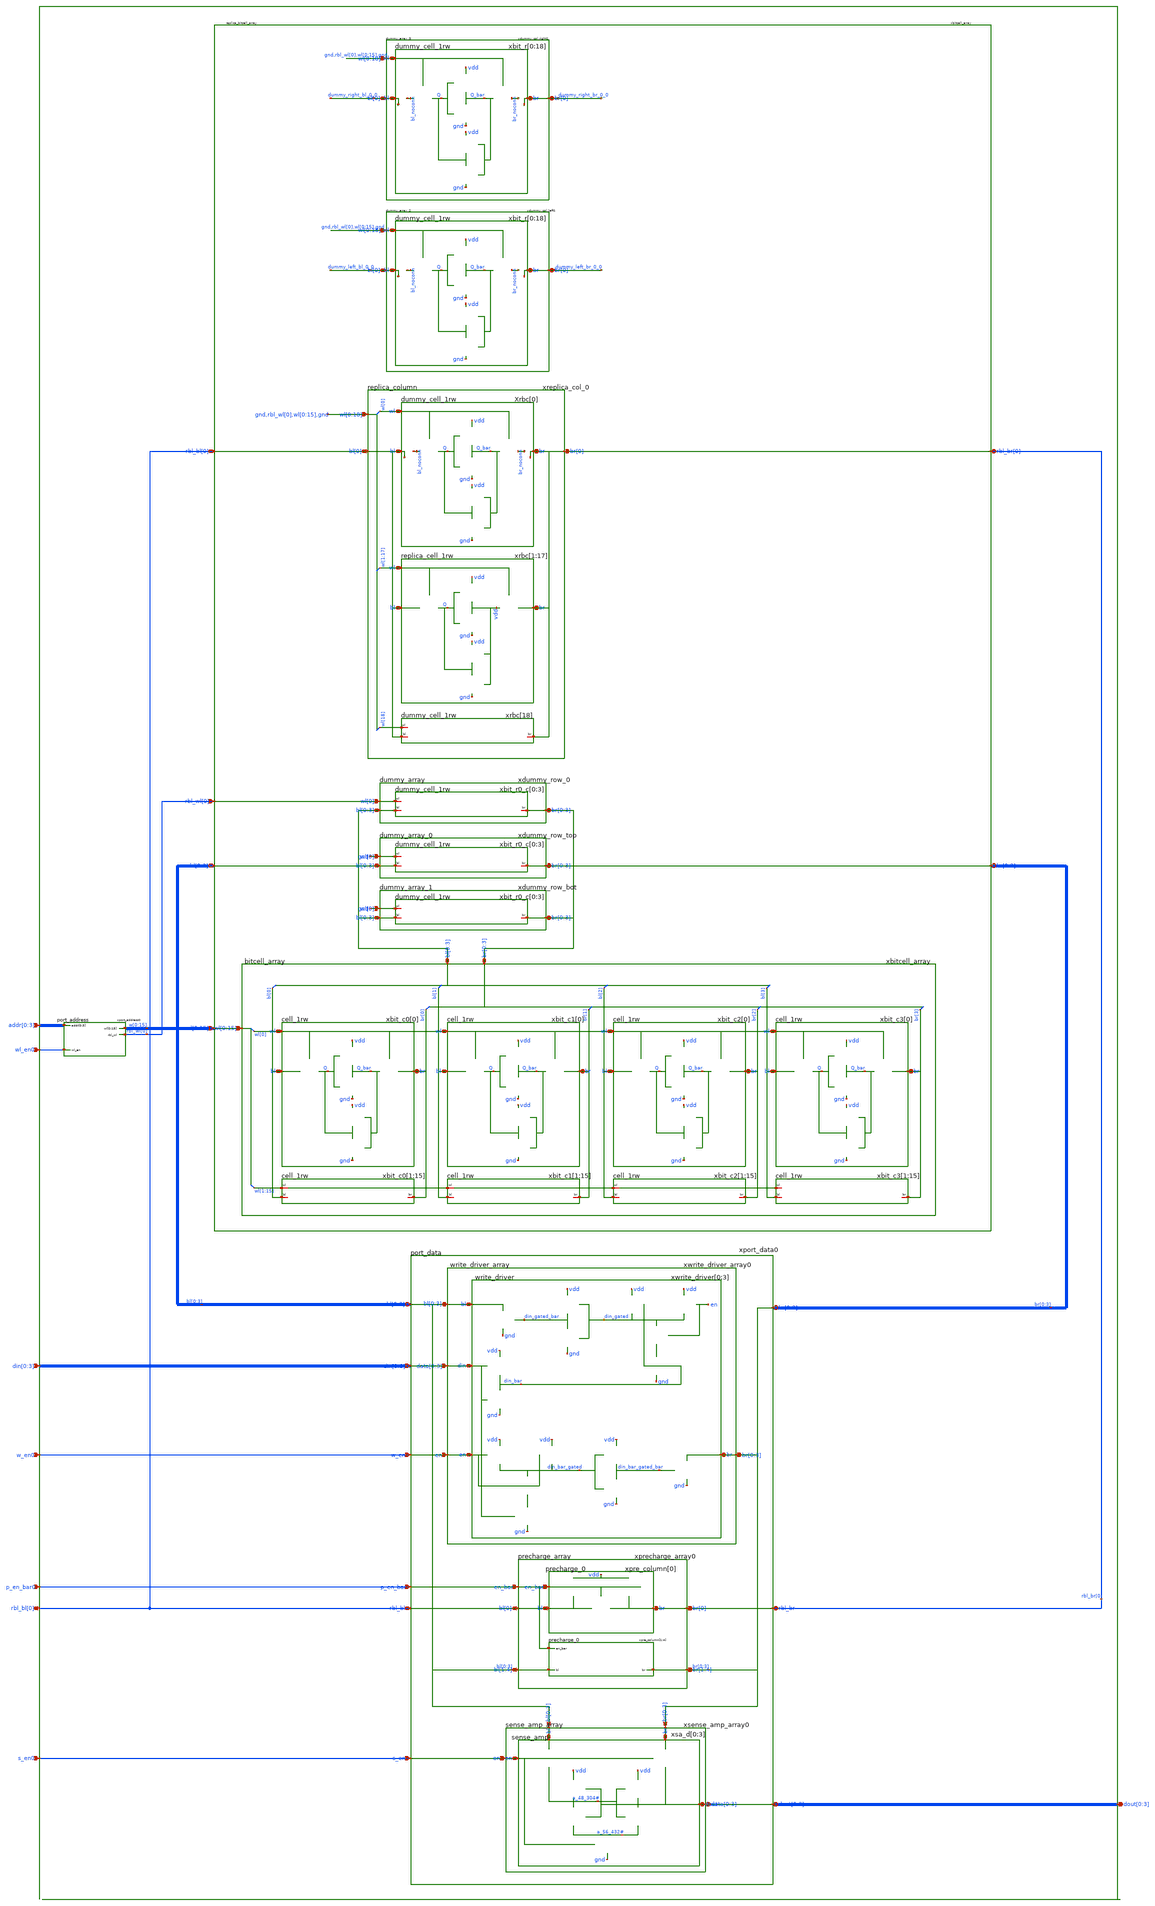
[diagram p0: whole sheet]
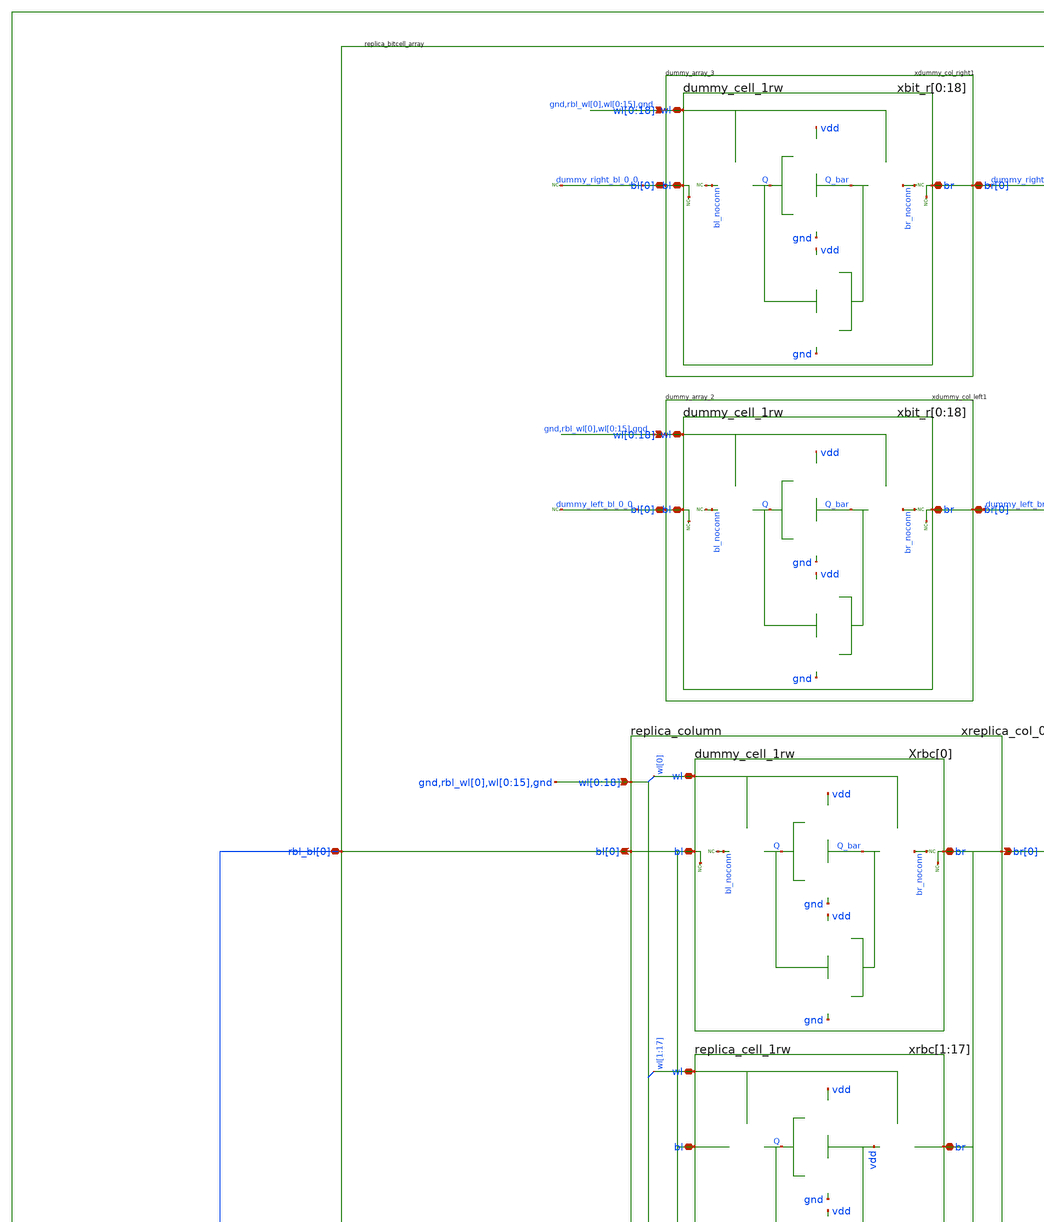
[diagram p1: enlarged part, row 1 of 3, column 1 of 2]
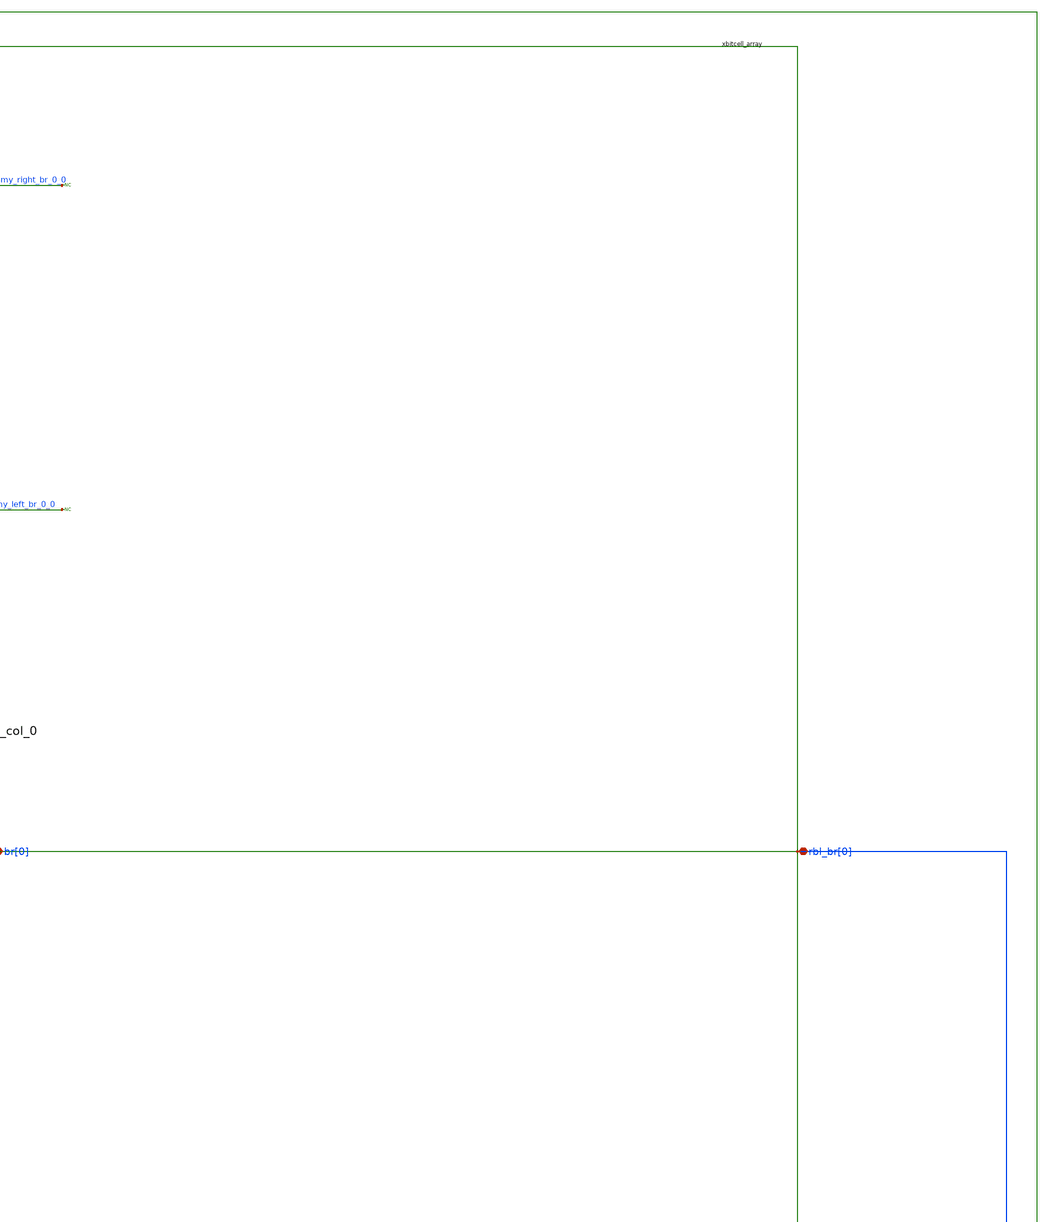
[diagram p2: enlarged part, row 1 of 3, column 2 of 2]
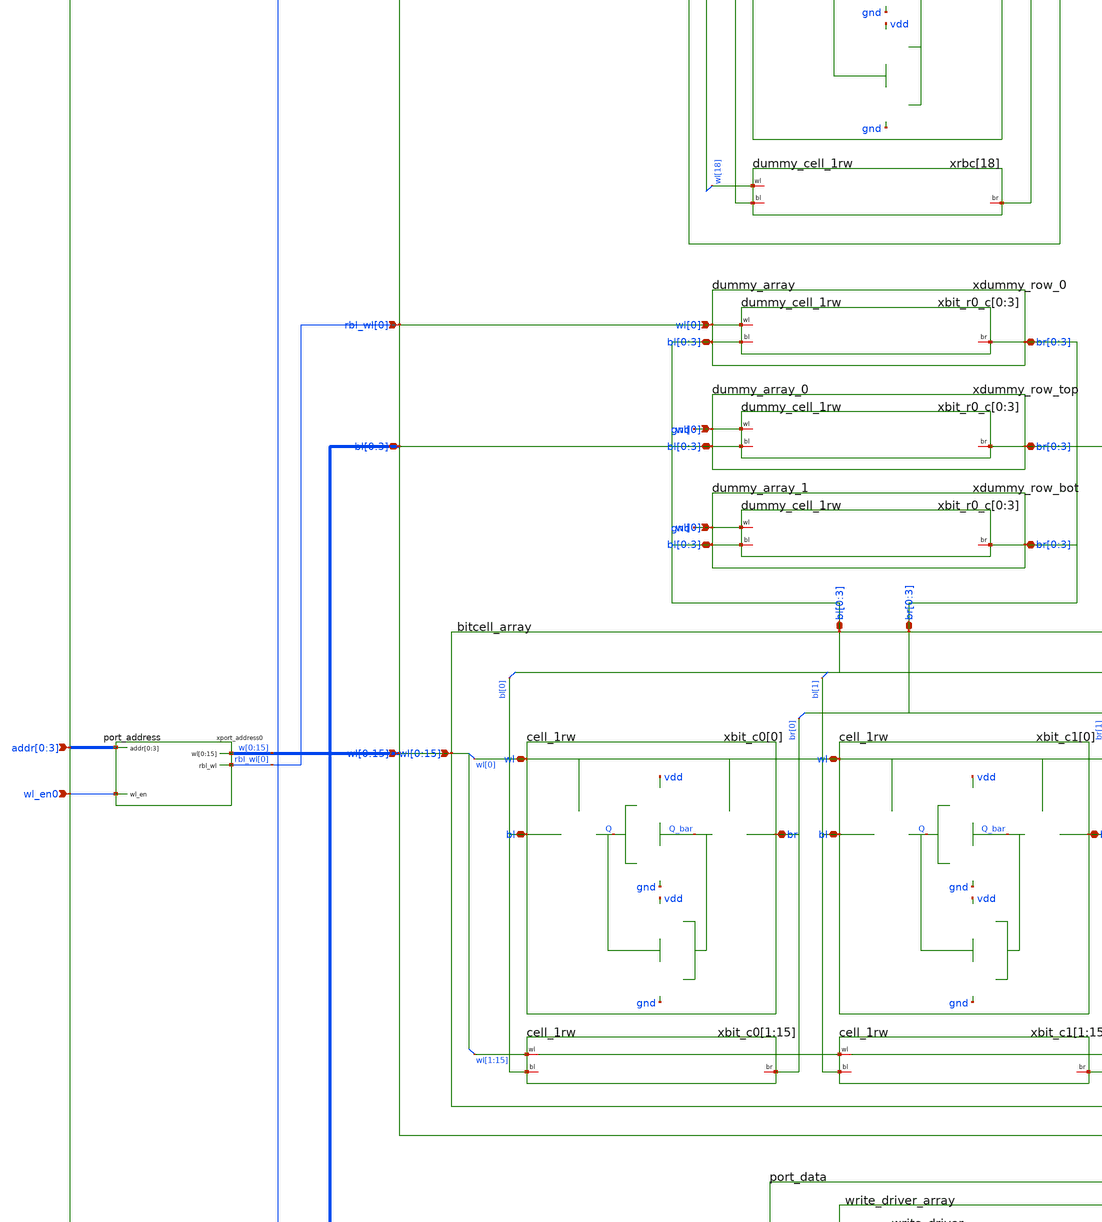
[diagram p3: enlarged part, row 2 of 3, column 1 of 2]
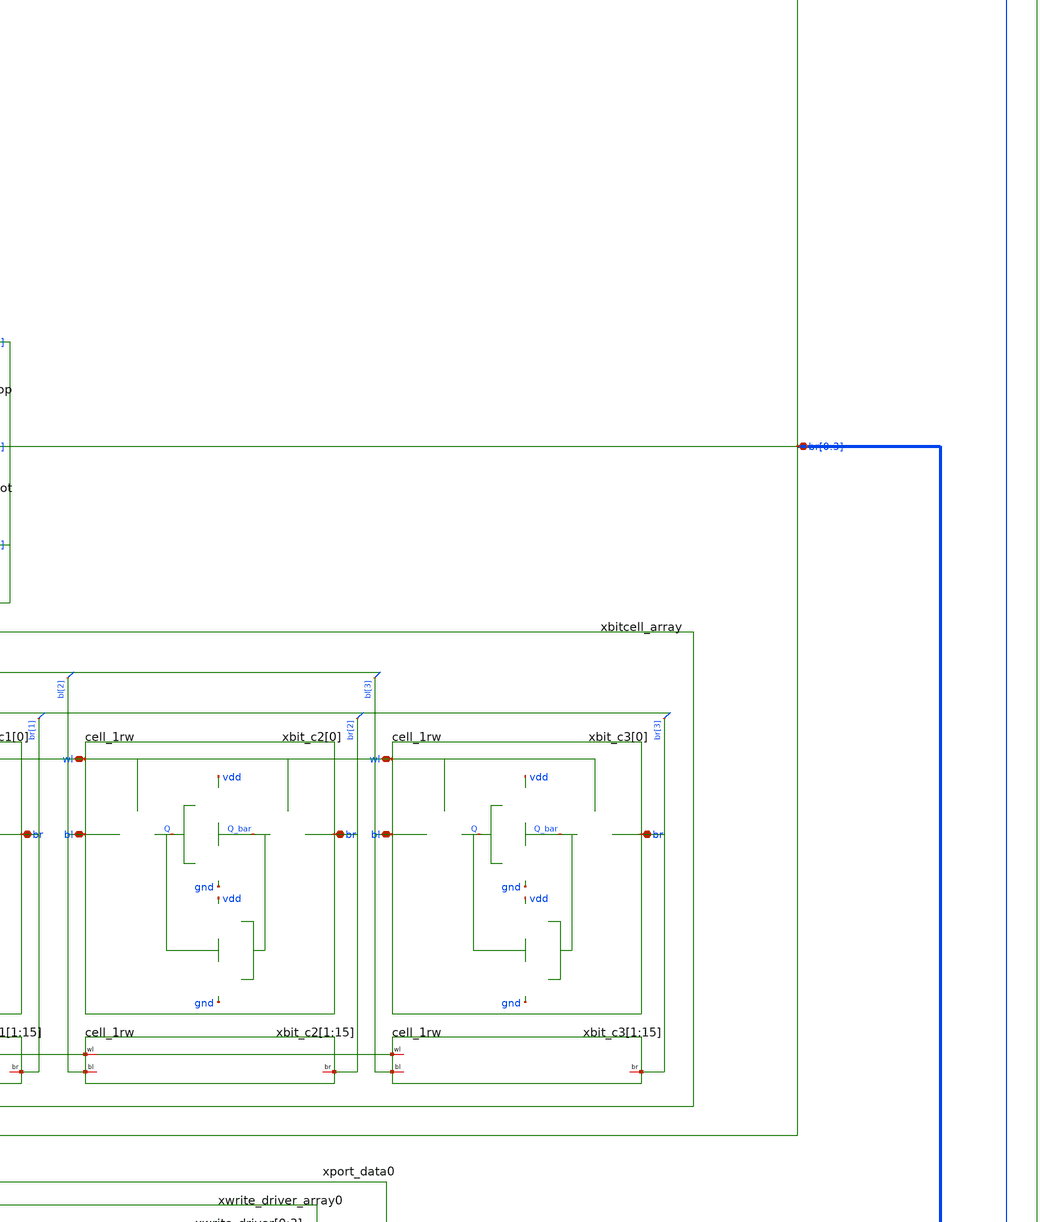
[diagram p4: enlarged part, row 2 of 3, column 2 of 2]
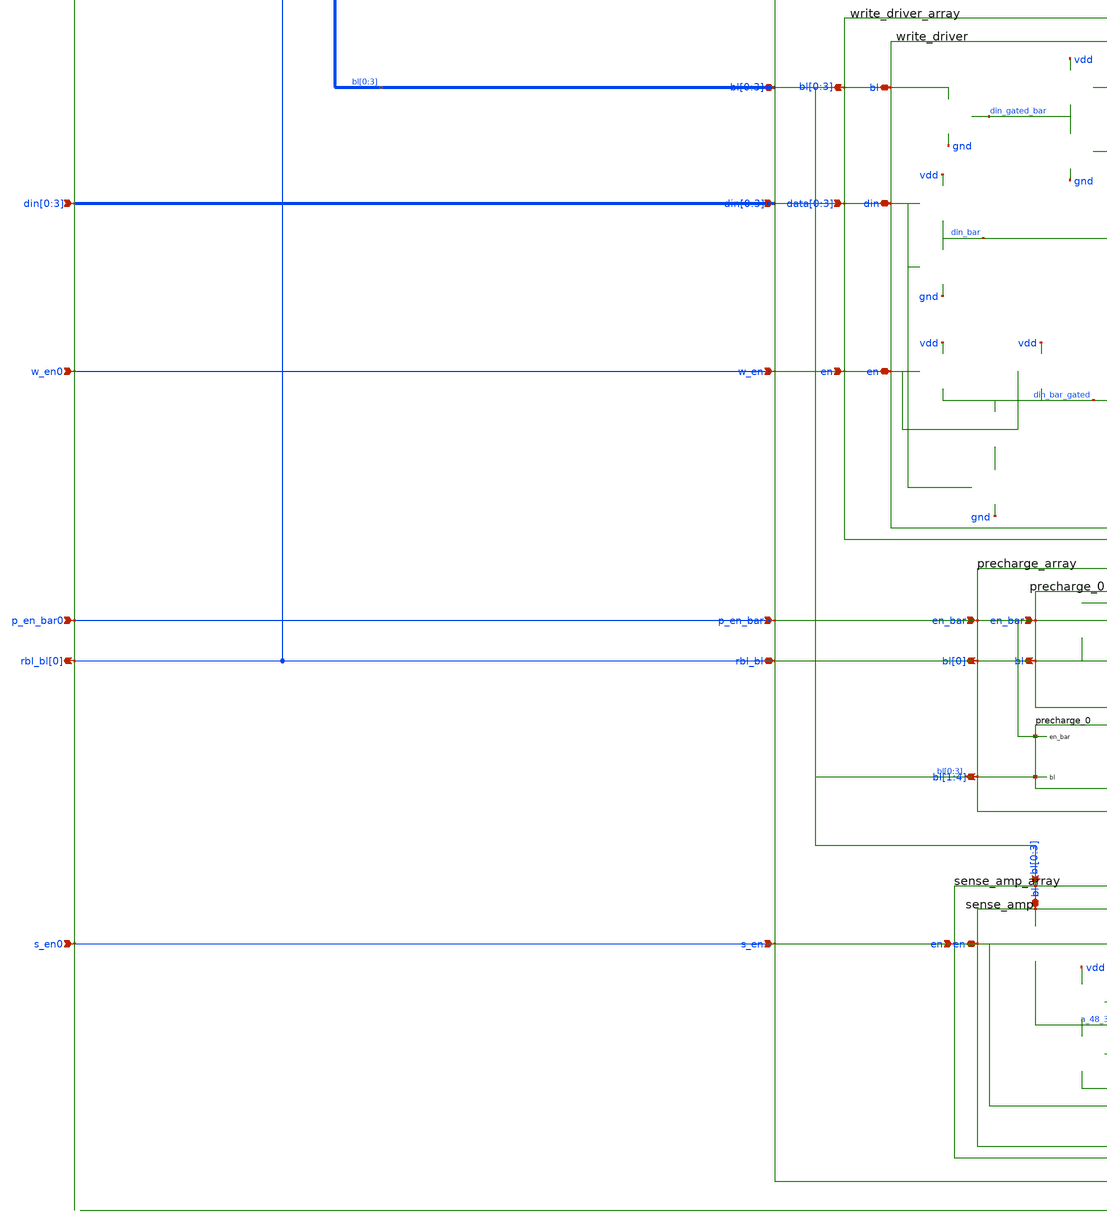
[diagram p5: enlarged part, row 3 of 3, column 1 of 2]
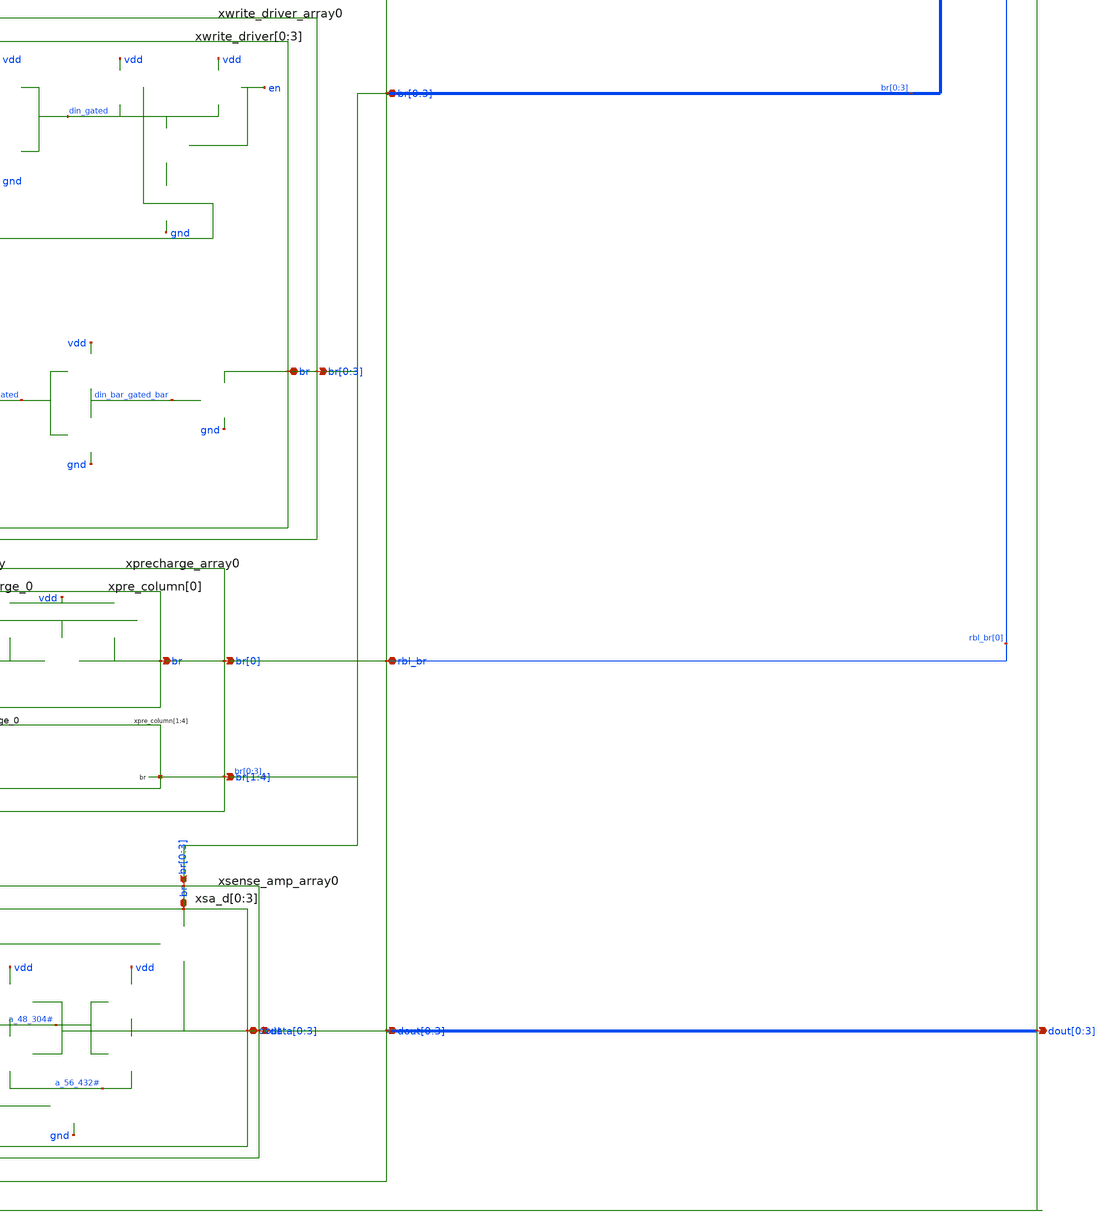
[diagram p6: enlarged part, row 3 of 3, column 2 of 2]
** sch_path: sram_4_16_scn4m/bank.sch
**.subckt bank dout[0],dout[1],dout[2],dout[3] rbl_bl[0] din[0],din[1],din[2],din[3]
*+ addr[0],addr[1],addr[2],addr[3] s_en0 p_en_bar0 w_en0 wl_en0
*.opin dout[0],dout[1],dout[2],dout[3]
*.opin rbl_bl[0]
*.ipin din[0],din[1],din[2],din[3]
*.ipin addr[0],addr[1],addr[2],addr[3]
*.ipin s_en0
*.ipin p_en_bar0
*.ipin w_en0
*.ipin wl_en0
xbitcell_array rbl_wl[0] rbl_bl[0] rbl_br[0] bl[0] bl[1] bl[2] bl[3] br[0] br[1] br[2] br[3] w[0]
+ w[1] w[2] w[3] w[4] w[5] w[6] w[7] w[8] w[9] w[10] w[11] w[12] w[13] w[14] w[15] vdd gnd
+ replica_bitcell_array
xport_data0 rbl_bl[0] rbl_br[0] bl[0] bl[1] bl[2] bl[3] br[0] br[1] br[2] br[3] dout[0] dout[1]
+ dout[2] dout[3] din[0] din[1] din[2] din[3] s_en0 p_en_bar0 w_en0 vdd gnd port_data
xport_address0 addr[0] addr[1] addr[2] addr[3] wl_en0 w[0] w[1] w[2] w[3] w[4] w[5] w[6] w[7] w[8]
+ w[9] w[10] w[11] w[12] w[13] w[14] w[15] rbl_wl[0] vdd gnd port_address
**.ends
.end
